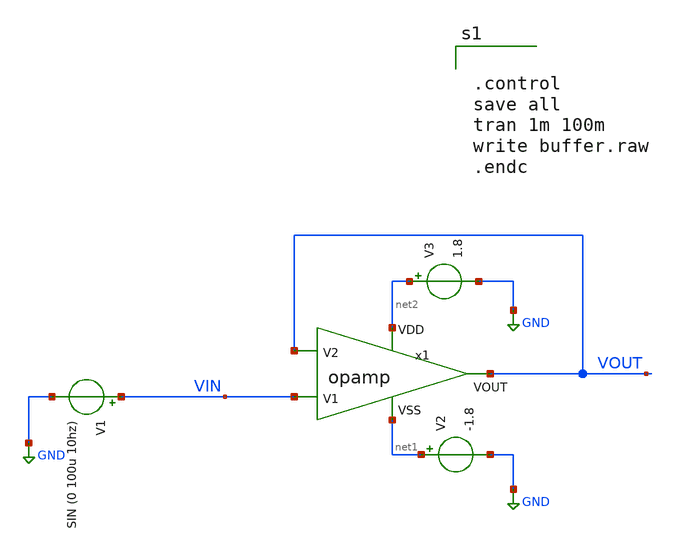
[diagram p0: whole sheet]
** sch_path: buffer.sch
**.subckt buffer
V1 VIN GND SIN (0 100u 10hz)
V3 net2 GND 1.8
V2 net1 GND -1.8
x1 net2 net1 VIN VOUT VOUT opamp
**** begin user architecture code

** opencircuitdesign pdks install
.lib $::SKYWATER_MODELS/sky130.lib.spice tt




.control
save all
tran 1m 100m
write buffer.raw
.endc


**** end user architecture code
**.ends

* expanding   symbol:  /foss/designs/chipalooza2024/sky130_hcmus_ip__instramp/opamp.sym # of pins=5
** sym_path: xschem/opamp.sym
** sch_path: xschem/opamp.sch
.subckt opamp VDD VSS V1 V2 VOUT
*.ipin VSS
*.ipin VDD
*.ipin V2
*.ipin V1
*.opin VOUT
XM2 net4 V2 net1 VSS sky130_fd_pr__nfet_g5v0d10v5 L=1 W=18 nf=1 ad='int((nf+1)/2) * W/nf * 0.29' as='int((nf+2)/2) * W/nf * 0.29'
+ pd='2*int((nf+1)/2) * (W/nf + 0.29)' ps='2*int((nf+2)/2) * (W/nf + 0.29)' nrd='0.29 / W' nrs='0.29 / W'
+ sa=0 sb=0 sd=0 mult=1 m=1
XM1 net5 net4 VDD VDD sky130_fd_pr__pfet_g5v0d10v5 L=1 W=30 nf=1 ad='int((nf+1)/2) * W/nf * 0.29' as='int((nf+2)/2) * W/nf * 0.29'
+ pd='2*int((nf+1)/2) * (W/nf + 0.29)' ps='2*int((nf+2)/2) * (W/nf + 0.29)' nrd='0.29 / W' nrs='0.29 / W'
+ sa=0 sb=0 sd=0 mult=1 m=1
XM4 net5 V1 net1 VSS sky130_fd_pr__nfet_g5v0d10v5 L=1 W=18 nf=1 ad='int((nf+1)/2) * W/nf * 0.29' as='int((nf+2)/2) * W/nf * 0.29'
+ pd='2*int((nf+1)/2) * (W/nf + 0.29)' ps='2*int((nf+2)/2) * (W/nf + 0.29)' nrd='0.29 / W' nrs='0.29 / W'
+ sa=0 sb=0 sd=0 mult=1 m=1
XM5 net1 net6 VSS VSS sky130_fd_pr__nfet_g5v0d10v5 L=1 W=15.171 nf=1 ad='int((nf+1)/2) * W/nf * 0.29'
+ as='int((nf+2)/2) * W/nf * 0.29' pd='2*int((nf+1)/2) * (W/nf + 0.29)' ps='2*int((nf+2)/2) * (W/nf + 0.29)'
+ nrd='0.29 / W' nrs='0.29 / W' sa=0 sb=0 sd=0 mult=1 m=1
XM6 VOUT net6 VSS VSS sky130_fd_pr__nfet_g5v0d10v5 L=1 W=19 nf=1 ad='int((nf+1)/2) * W/nf * 0.29' as='int((nf+2)/2) * W/nf * 0.29'
+ pd='2*int((nf+1)/2) * (W/nf + 0.29)' ps='2*int((nf+2)/2) * (W/nf + 0.29)' nrd='0.29 / W' nrs='0.29 / W'
+ sa=0 sb=0 sd=0 mult=1 m=1
XM7 net6 net6 VSS VSS sky130_fd_pr__nfet_g5v0d10v5 L=1 W=20 nf=1 ad='int((nf+1)/2) * W/nf * 0.29' as='int((nf+2)/2) * W/nf * 0.29'
+ pd='2*int((nf+1)/2) * (W/nf + 0.29)' ps='2*int((nf+2)/2) * (W/nf + 0.29)' nrd='0.29 / W' nrs='0.29 / W'
+ sa=0 sb=0 sd=0 mult=1 m=1
XM3 net4 net4 VDD VDD sky130_fd_pr__pfet_g5v0d10v5 L=1 W=30 nf=1 ad='int((nf+1)/2) * W/nf * 0.29' as='int((nf+2)/2) * W/nf * 0.29'
+ pd='2*int((nf+1)/2) * (W/nf + 0.29)' ps='2*int((nf+2)/2) * (W/nf + 0.29)' nrd='0.29 / W' nrs='0.29 / W'
+ sa=0 sb=0 sd=0 mult=1 m=1
XM8 VOUT net5 VDD VDD sky130_fd_pr__pfet_g5v0d10v5 L=1 W=38 nf=1 ad='int((nf+1)/2) * W/nf * 0.29' as='int((nf+2)/2) * W/nf * 0.29'
+ pd='2*int((nf+1)/2) * (W/nf + 0.29)' ps='2*int((nf+2)/2) * (W/nf + 0.29)' nrd='0.29 / W' nrs='0.29 / W'
+ sa=0 sb=0 sd=0 mult=2 m=2
XC1 net7 net5 sky130_fd_pr__cap_mim_m3_1 W=5.5 L=10 MF=10 m=10
V_ibias net8 net6 0
.save i(v_ibias)
XR5 net2 VDD VSS sky130_fd_pr__res_high_po_0p69 L=18.58 mult=1 m=1
XR1 net3 net2 VSS sky130_fd_pr__res_high_po_0p69 L=18.58 mult=1 m=1
XR2 net8 net3 VSS sky130_fd_pr__res_high_po_0p69 L=18.58 mult=1 m=1
XR3 net7 VOUT VSS sky130_fd_pr__res_high_po_0p69 L=2.41 mult=1 m=1
.ends

.GLOBAL GND
.end
